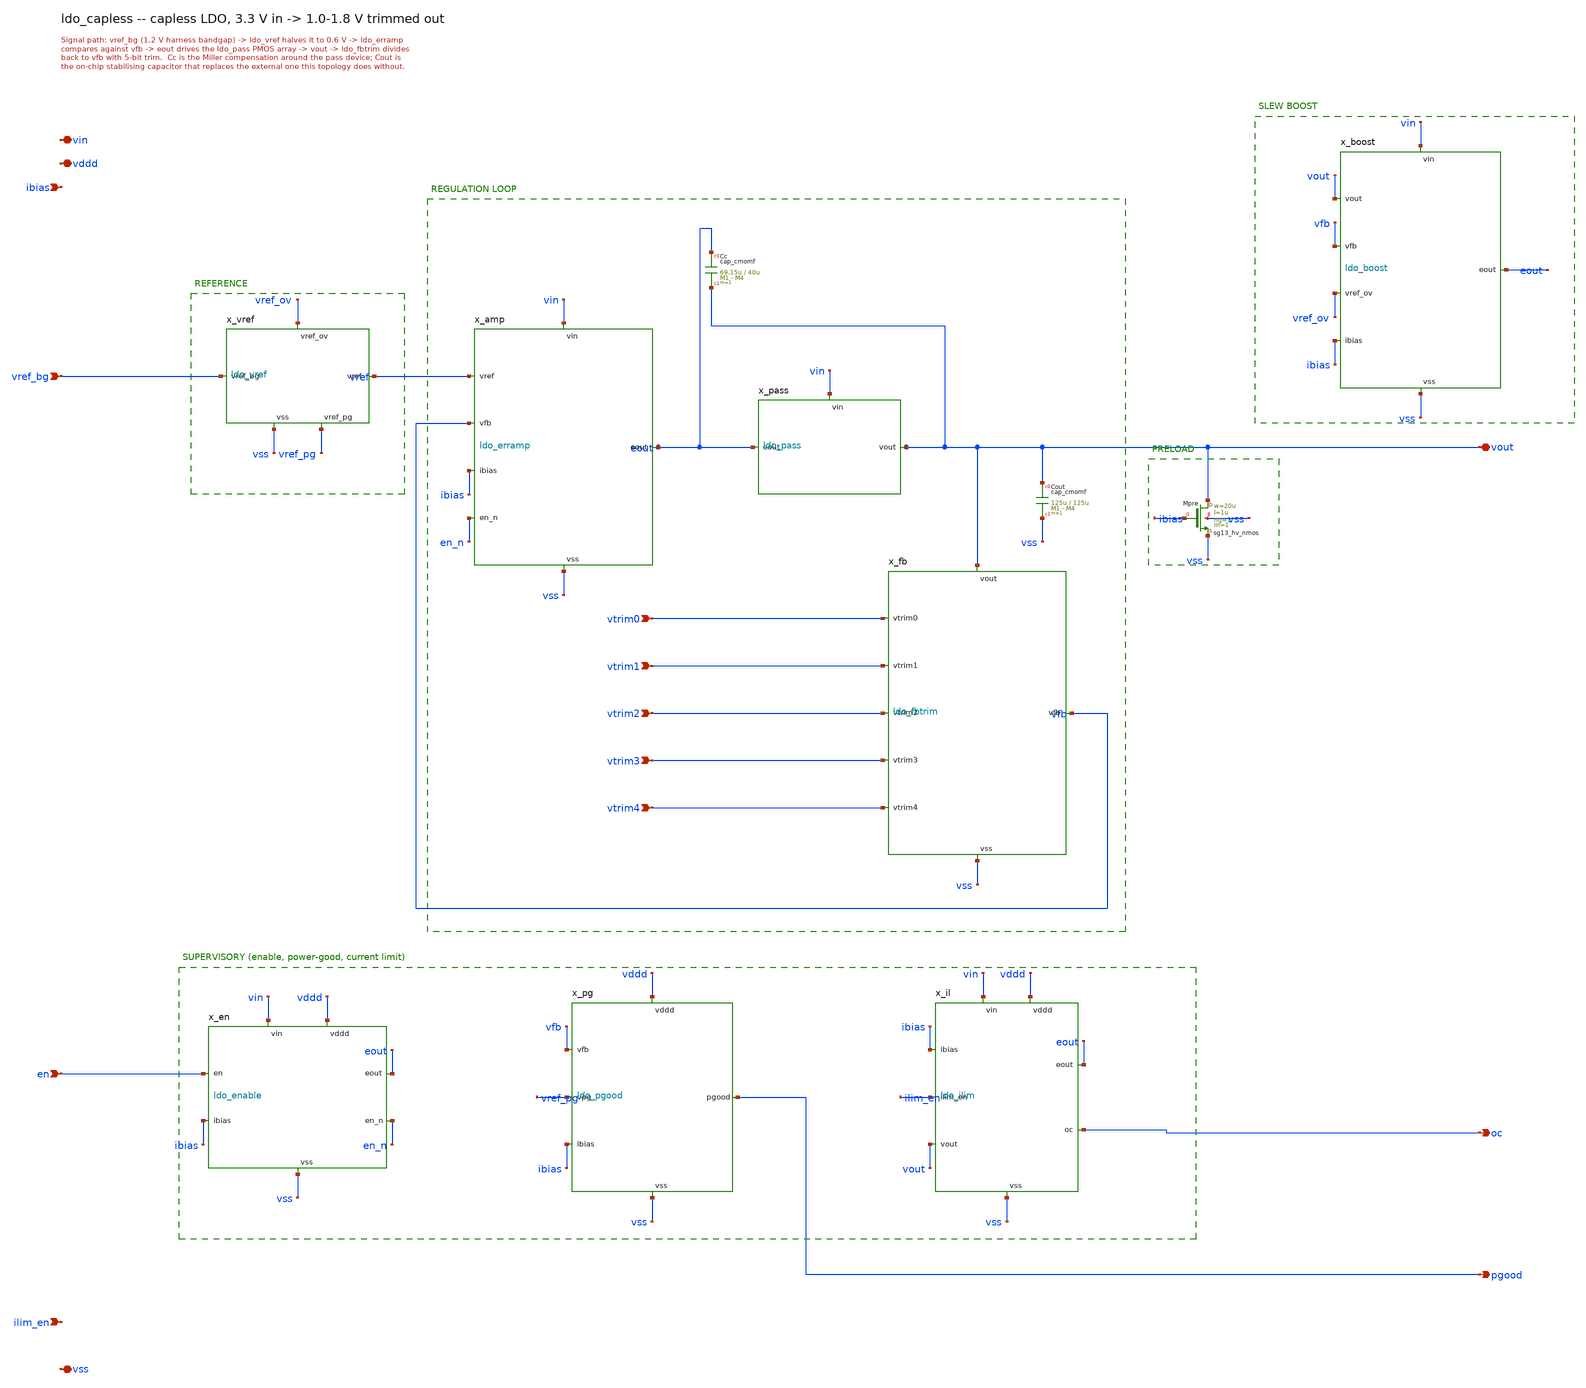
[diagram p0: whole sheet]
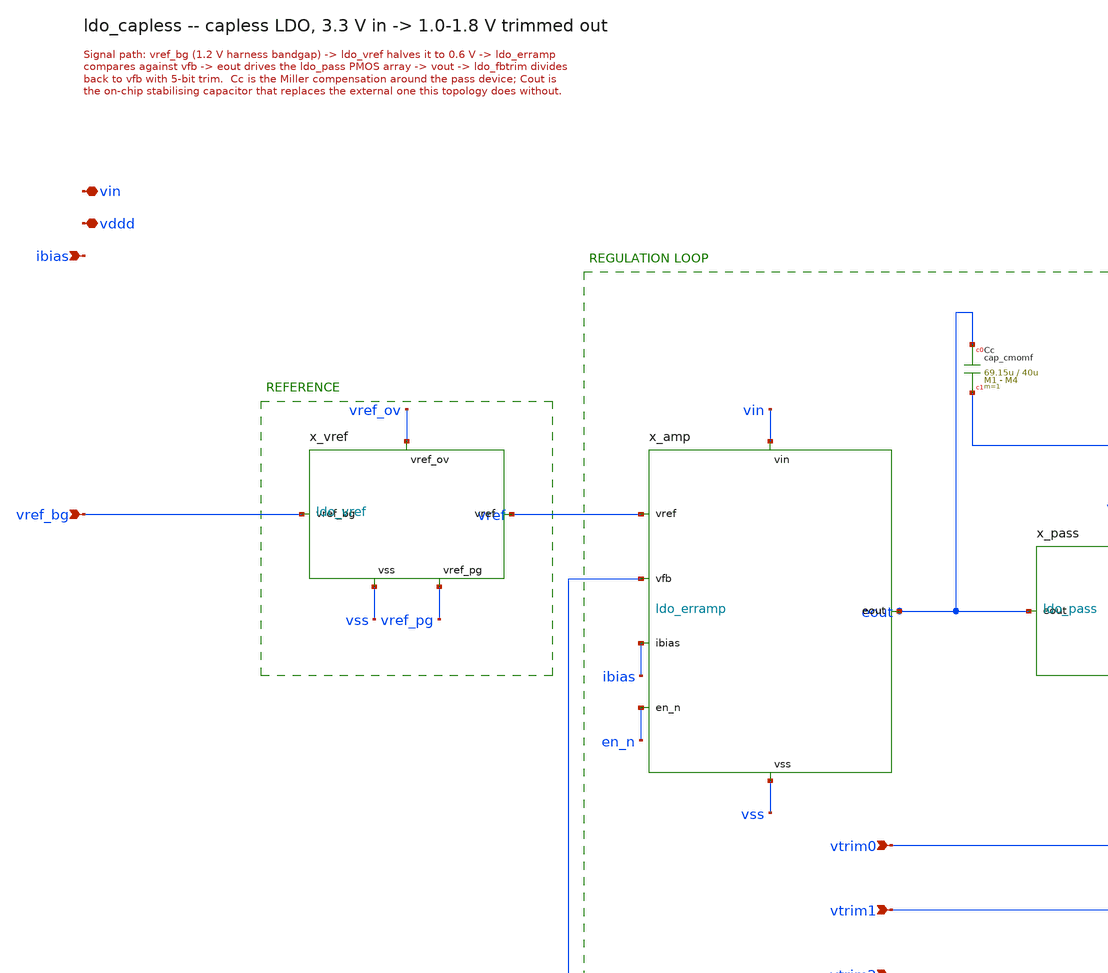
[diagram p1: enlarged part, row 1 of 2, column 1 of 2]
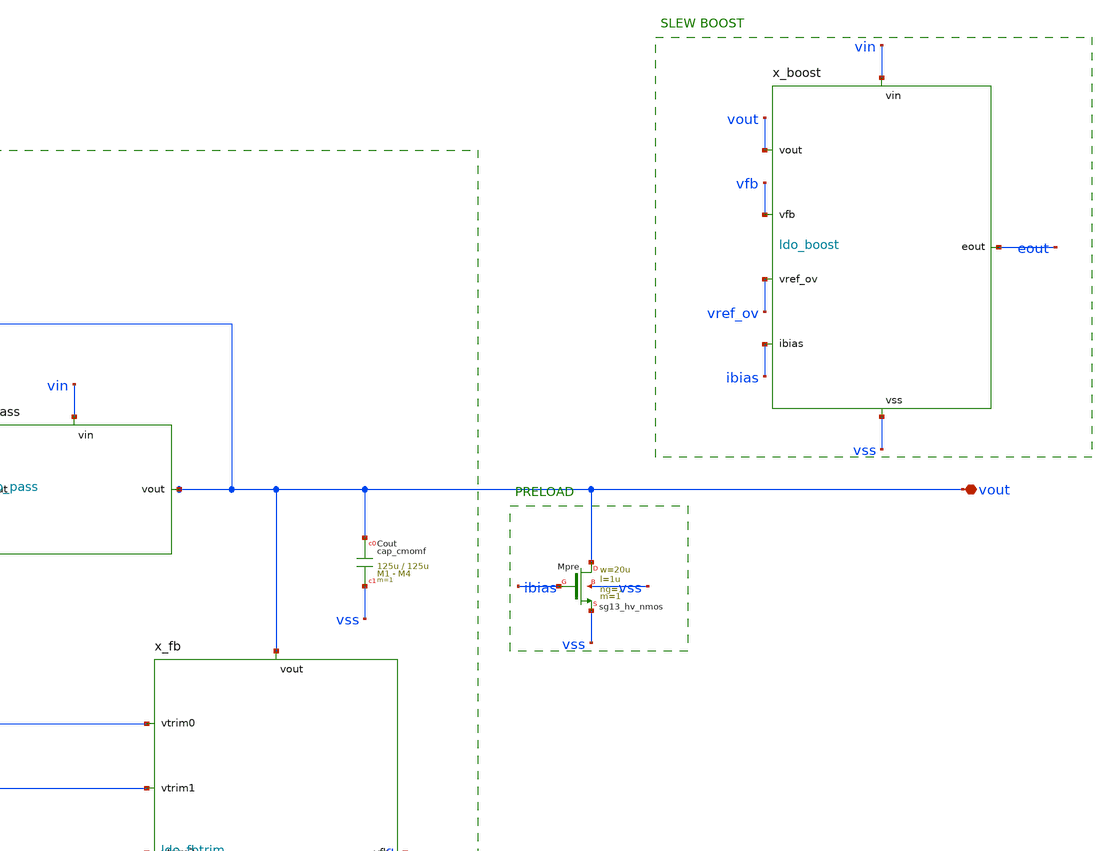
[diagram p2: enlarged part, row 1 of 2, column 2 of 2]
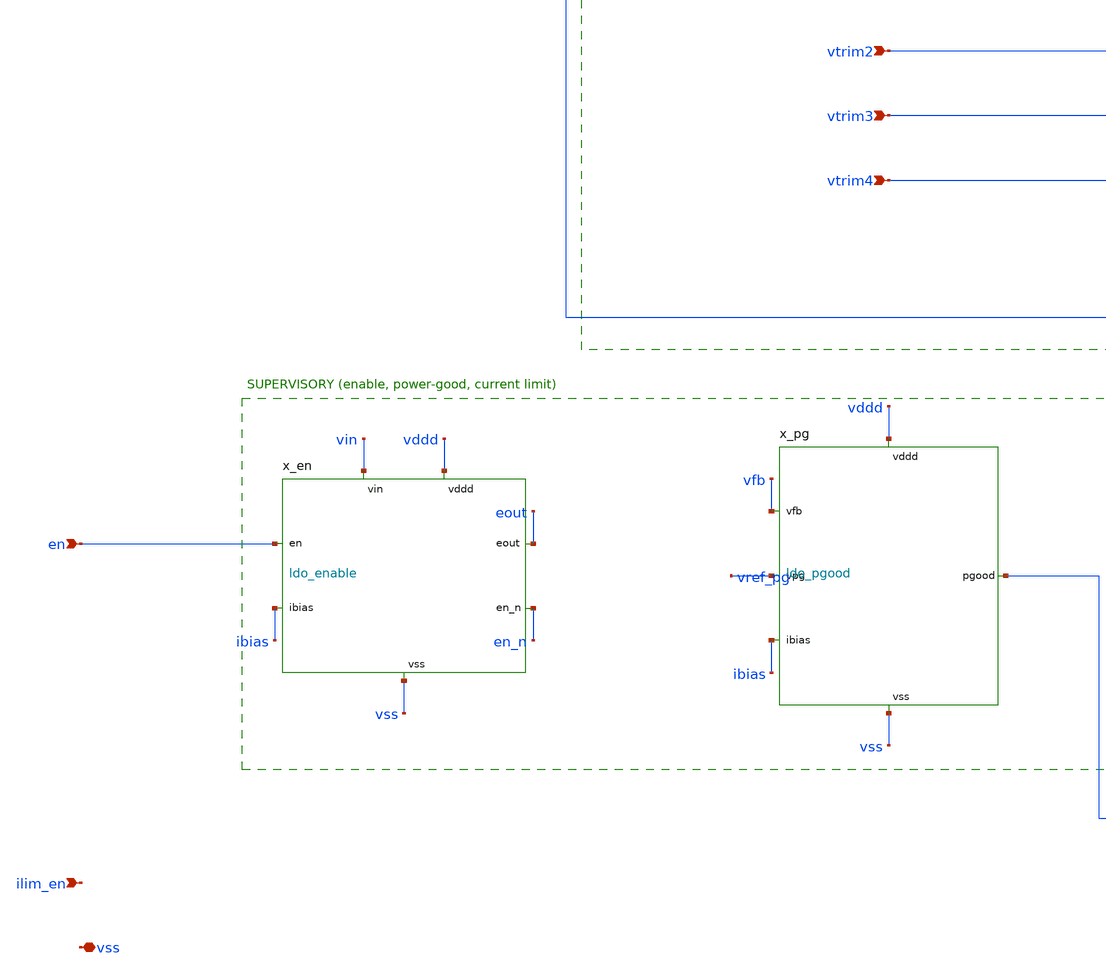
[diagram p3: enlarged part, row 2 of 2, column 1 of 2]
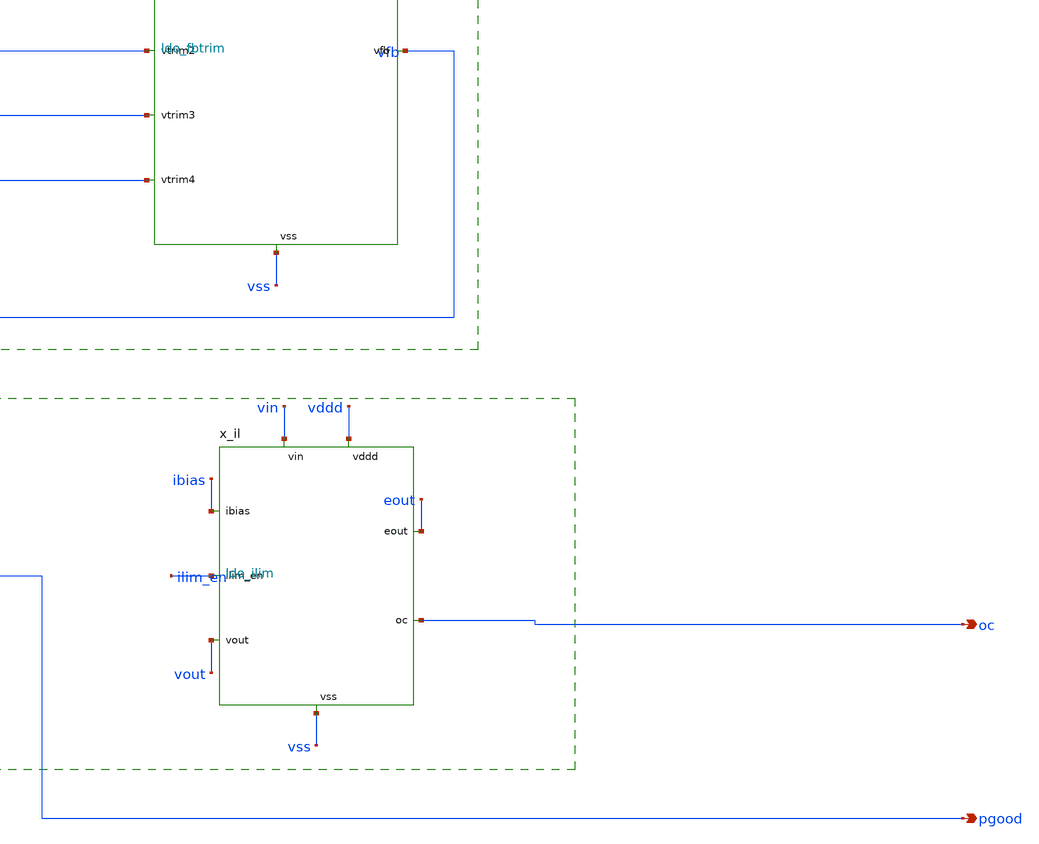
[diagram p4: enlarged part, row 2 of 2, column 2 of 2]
** sch_path: xschem/ldo_capless.sch
**.subckt ldo_capless vin vout vref_bg ibias en vddd vss pgood ilim_en oc vtrim0 vtrim1 vtrim2
*+ vtrim3 vtrim4
*.iopin vin
*.iopin vout
*.ipin vref_bg
*.ipin ibias
*.ipin en
*.iopin vddd
*.iopin vss
*.opin pgood
*.ipin ilim_en
*.opin oc
*.ipin vtrim0
*.ipin vtrim1
*.ipin vtrim2
*.ipin vtrim3
*.ipin vtrim4
x_vref vref_bg vref vref_ov vss vref_pg ldo_vref
x_amp vref vfb ibias en_n eout vin vss ldo_erramp
x_pass eout vout vin ldo_pass
x_fb vtrim0 vtrim1 vtrim2 vtrim3 vtrim4 vfb vout vss ldo_fbtrim
XCc eout vout cap_cmomf w=69.15u l=40u mmin=1 mmax=4 subblock=0 rfmodel=0 subscale=1 m=1 mm_ok=1
x_boost vout vfb vref_ov ibias eout vin vss ldo_boost
XMpre vout ibias vss vss sg13_hv_nmos w=20u l=1u ng=1 m=1 mm_ok=1
x_en en ibias eout en_n vin vddd vss ldo_enable
x_pg vfb vref_pg ibias pgood vddd vss ldo_pgood
x_il ibias ilim_en vout eout oc vin vddd vss ldo_ilim
XCout vout vss cap_cmomf w=125u l=125u mmin=1 mmax=4 subblock=0 rfmodel=0 subscale=1 m=1 mm_ok=1
**.ends

* expanding   symbol:  ldo_vref.sym # of pins=5
** sym_path: xschem/ldo_vref.sym
** sch_path: xschem/ldo_vref.sch
.subckt ldo_vref vref_bg vref vref_ov vss vref_pg
*.ipin vref_bg
*.opin vref
*.opin vref_pg
*.iopin vss
*.opin vref_ov
XR1a vref_bg vref_ov sub! rhigh w=1u l=194.4u m=1 b=0 mm_ok=1
XR1b vref_ov vref sub! rhigh w=1u l=17.6u m=1 b=0 mm_ok=1
XR2a vref vref_pg sub! rhigh w=1u l=21.1u m=1 b=0 mm_ok=1
XR2b vref_pg vss sub! rhigh w=1u l=190.5u m=1 b=0 mm_ok=1
XCf vref vss cap_cmomf w=10u l=10u mmin=1 mmax=4 subblock=0 rfmodel=0 subscale=1 m=1 mm_ok=1
.ends


* expanding   symbol:  ldo_erramp.sym # of pins=7
** sym_path: xschem/ldo_erramp.sym
** sch_path: xschem/ldo_erramp.sch
.subckt ldo_erramp vref vfb ibias en_n eout vin vss
*.ipin vref
*.ipin vfb
*.ipin ibias
*.ipin en_n
*.opin eout
*.iopin vin
*.iopin vss
XMp0 pbias pbias vin vin sg13_hv_pmos w=4u l=1u ng=1 m=1 mm_ok=1
XMtail ptail pbias vin vin sg13_hv_pmos w=4u l=1u ng=1 m=1 mm_ok=1
XM1 n3 vref ptail vin sg13_hv_pmos w=2.5u l=1u ng=1 m=1 mm_ok=1
XM2 eout1 vfb ptail vin sg13_hv_pmos w=2.5u l=1u ng=1 m=1 mm_ok=1
XM3 n3 n3 vss vss sg13_hv_nmos w=10u l=1u ng=1 m=1 mm_ok=1
XM4 eout1 n3 vss vss sg13_hv_nmos w=10u l=1u ng=1 m=1 mm_ok=1
XM5 eout eout1 vss vss sg13_hv_nmos w=10u l=1u ng=1 m=1 mm_ok=1
XM6 eout pbias vin vin sg13_hv_pmos w=2u l=1u ng=1 m=1 mm_ok=1
XCm eout nzc cap_cmomf w=193u l=193u mmin=1 mmax=4 subblock=0 rfmodel=0 subscale=1 m=1 mm_ok=1
XRz nzc eout1 sub! rhigh w=1u l=40.48u m=1 b=0 mm_ok=1
XMen1 eout1 en_n vss vss sg13_lv_nmos w=5u l=0.13u ng=1 m=1 mm_ok=1
XMn1 pbias ibias vss vss sg13_hv_nmos w=20u l=1u ng=1 m=1 mm_ok=1
XMr ibias ibias vss vss sg13_hv_nmos w=2u l=1u ng=1 m=1 mm_ok=1
.ends


* expanding   symbol:  ldo_pass.sym # of pins=3
** sym_path: xschem/ldo_pass.sym
** sch_path: xschem/ldo_pass.sch
.subckt ldo_pass eout vout vin
*.ipin eout
*.iopin vin
*.iopin vout
XMpass vout eout vin vin sg13_hv_pmos w=100u l=0.5u ng=1 m=64 mm_ok=1
.ends


* expanding   symbol:  ldo_fbtrim.sym # of pins=8
** sym_path: xschem/ldo_fbtrim.sym
** sch_path: xschem/ldo_fbtrim.sch
.subckt ldo_fbtrim vtrim0 vtrim1 vtrim2 vtrim3 vtrim4 vfb vout vss
*.iopin vout
*.opin vfb
*.iopin vss
*.ipin vtrim0
*.ipin vtrim1
*.ipin vtrim2
*.ipin vtrim3
*.ipin vtrim4
XRtop vout vfb sub! rhigh w=1u l=212u m=1 b=0 mm_ok=1
XRbase vfb t0 sub! rhigh w=1u l=106u m=1 b=0 mm_ok=1
XRt0 t0 t1 sub! rhigh w=1u l=6.8u m=1 b=0 mm_ok=1
XMsw0 t0 vtrim0 t1 vss sg13_lv_nmos w=20u l=0.13u ng=1 m=1 mm_ok=1
XRt1 t1 t2 sub! rhigh w=1u l=13.6u m=1 b=0 mm_ok=1
XMsw1 t1 vtrim1 t2 vss sg13_lv_nmos w=20u l=0.13u ng=1 m=1 mm_ok=1
XRt2 t2 t3 sub! rhigh w=1u l=27.3u m=1 b=0 mm_ok=1
XMsw2 t2 vtrim2 t3 vss sg13_lv_nmos w=20u l=0.13u ng=1 m=1 mm_ok=1
XRt3 t3 t4 sub! rhigh w=1u l=54.6u m=1 b=0 mm_ok=1
XMsw3 t3 vtrim3 t4 vss sg13_lv_nmos w=20u l=0.13u ng=1 m=1 mm_ok=1
XRt4 t4 vss sub! rhigh w=1u l=109.1u m=1 b=0 mm_ok=1
XMsw4 t4 vtrim4 vss vss sg13_lv_nmos w=20u l=0.13u ng=1 m=1 mm_ok=1
.ends


* expanding   symbol:  ldo_boost.sym # of pins=7
** sym_path: xschem/ldo_boost.sym
** sch_path: xschem/ldo_boost.sch
.subckt ldo_boost vout vfb vref_ov ibias eout vin vss
*.ipin vout
*.ipin vfb
*.ipin vref_ov
*.ipin ibias
*.iopin eout
*.iopin vin
*.iopin vss
XMbn nbd ibias vss vss sg13_hv_nmos w=4u l=1u ng=1 m=1 mm_ok=1
XMbp nbd nbd vin vin sg13_hv_pmos w=4u l=1u ng=1 m=1 mm_ok=1
XMpl nbl nbd vin vin sg13_hv_pmos w=2u l=1u ng=1 m=1 mm_ok=1
XMrb nbl nbl vss vss sg13_hv_nmos w=2u l=1u ng=1 m=1 mm_ok=1
XMct ptb nbd vin vin sg13_hv_pmos w=4u l=1u ng=1 m=1 mm_ok=1
XMc1 ncd vfb ptb vin sg13_hv_pmos w=5u l=1u ng=1 m=1 mm_ok=1
XMc2 nx vref_ov ptb vin sg13_hv_pmos w=5u l=1u ng=1 m=1 mm_ok=1
XMc3 ncd ncd vss vss sg13_hv_nmos w=10u l=1u ng=1 m=1 mm_ok=1
XMc4 nx ncd vss vss sg13_hv_nmos w=10u l=1u ng=1 m=1 mm_ok=1
XMc6 ng nbd vin vin sg13_hv_pmos w=2u l=1u ng=1 m=1 mm_ok=1
XMc5 ng nx vss vss sg13_hv_nmos w=10u l=1u ng=1 m=1 mm_ok=1
XCb vout nb cap_cmomf w=28u l=28u mmin=1 mmax=4 subblock=0 rfmodel=0 subscale=1 m=1 mm_ok=1
XRb nb nbl sub! rhigh w=1u l=2940u m=1 b=0 mm_ok=1
XMnb nx2 nb vss vss sg13_hv_nmos w=1u l=4u ng=1 m=1 mm_ok=1
XRnx vin nx2 sub! rhigh w=1u l=735u m=1 b=0 mm_ok=1
XMve nmid ng vin vin sg13_hv_pmos w=40u l=0.5u ng=1 m=1 mm_ok=1
XMpb eout nx2 nmid vin sg13_hv_pmos w=20u l=0.5u ng=1 m=1 mm_ok=1
.ends


* expanding   symbol:  ldo_enable.sym # of pins=7
** sym_path: xschem/ldo_enable.sym
** sch_path: xschem/ldo_enable.sch
.subckt ldo_enable en ibias eout en_n vin vddd vss
*.ipin en
*.opin en_n
*.iopin ibias
*.iopin eout
*.iopin vin
*.iopin vddd
*.iopin vss
Xinv en_n en vddd vss sg13cmos5l_inv_1
XMen_bias ibias en_n vss vss sg13_lv_nmos w=10u l=0.13u ng=1 m=1 mm_ok=1
XRls vin ls sub! rhigh w=1u l=700u m=1 b=0 mm_ok=1
XMls ls en_n vss vss sg13_hv_nmos w=10u l=0.5u ng=1 m=1 mm_ok=1
XMdis eout ls vin vin sg13_hv_pmos w=20u l=0.5u ng=1 m=1 mm_ok=1
.ends


* expanding   symbol:  ldo_pgood.sym # of pins=6
** sym_path: xschem/ldo_pgood.sym
** sch_path: xschem/ldo_pgood.sch
.subckt ldo_pgood vfb vpg ibias pgood vddd vss
*.ipin vfb
*.ipin vpg
*.ipin ibias
*.opin pgood
*.iopin vddd
*.iopin vss
XM1 cn vpg ptail vss sg13_lv_nmos w=10u l=0.5u ng=1 m=1 mm_ok=1
XM2 cmp vfb ptail vss sg13_lv_nmos w=10u l=0.5u ng=1 m=1 mm_ok=1
XM3 cn cn vddd vddd sg13_lv_pmos w=10u l=0.5u ng=1 m=1 mm_ok=1
XM4 cmp cn vddd vddd sg13_lv_pmos w=10u l=0.5u ng=1 m=1 mm_ok=1
XMt ptail ibias vss vss sg13_lv_nmos w=40u l=0.5u ng=1 m=1 mm_ok=1
Xout pgood cmp vddd vss sg13cmos5l_inv_2
.ends


* expanding   symbol:  ldo_ilim.sym # of pins=8
** sym_path: xschem/ldo_ilim.sym
** sch_path: xschem/ldo_ilim.sch
.subckt ldo_ilim ibias ilim_en vout eout oc vin vddd vss
*.iopin eout
*.ipin vout
*.ipin ibias
*.ipin ilim_en
*.opin oc
*.iopin vin
*.iopin vddd
*.iopin vss
XMsense sense_d eout vin vin sg13_hv_pmos w=2u l=0.5u ng=1 m=1 mm_ok=1
XMsd sense_d ibias vss vss sg13_hv_nmos w=1u l=4u ng=1 m=1 mm_ok=1
XMcas oc_n vout sense_d vin sg13_hv_pmos w=4u l=0.5u ng=1 m=1 mm_ok=1
XMref oc_n ibias vss vss sg13_hv_nmos w=50u l=1u ng=1 m=1 mm_ok=1
XMdis_oc oc_n ilim_en_n vss vss sg13_hv_nmos w=10u l=0.5u ng=1 m=1 mm_ok=1
Xinv_ie ilim_en_n ilim_en vddd vss sg13cmos5l_inv_1
XMocp oc_nb oc_n vin vin sg13_hv_pmos w=4u l=0.5u ng=1 m=1 mm_ok=1
XMocn oc_nb oc_n vss vss sg13_hv_nmos w=2u l=0.5u ng=1 m=1 mm_ok=1
XMlim eout oc_nb vin vin sg13_hv_pmos w=20u l=0.5u ng=1 m=1 mm_ok=1
XRoc vddd oc_lv sub! rhigh w=1u l=140u m=1 b=0 mm_ok=1
XMoc oc_lv oc_n vss vss sg13_hv_nmos w=10u l=0.5u ng=1 m=1 mm_ok=1
Xinv_oc oc oc_lv vddd vss sg13cmos5l_inv_2
.ends

.end
